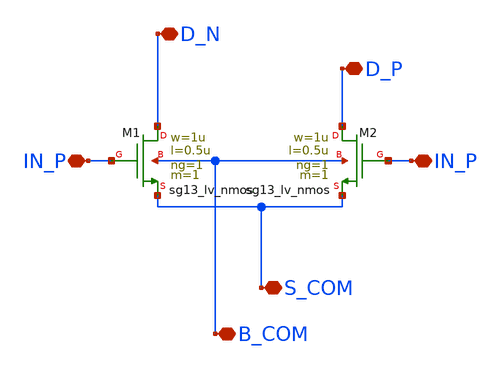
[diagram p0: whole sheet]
** sch_path: xschem/Proyecto/klayout/diff_pair_clase.sch
**.subckt diff_pair_clase D_N D_P S_COM B_COM IN_P IN_P
*.iopin D_N
*.iopin D_P
*.iopin S_COM
*.iopin B_COM
*.iopin IN_P
*.iopin IN_P
XM1 D_N IN_P S_COM B_COM sg13_lv_nmos w=1u l=0.5u ng=1 m=1 mm_ok=1
XM2 D_P IN_P S_COM B_COM sg13_lv_nmos w=1u l=0.5u ng=1 m=1 mm_ok=1
**.ends
.end
